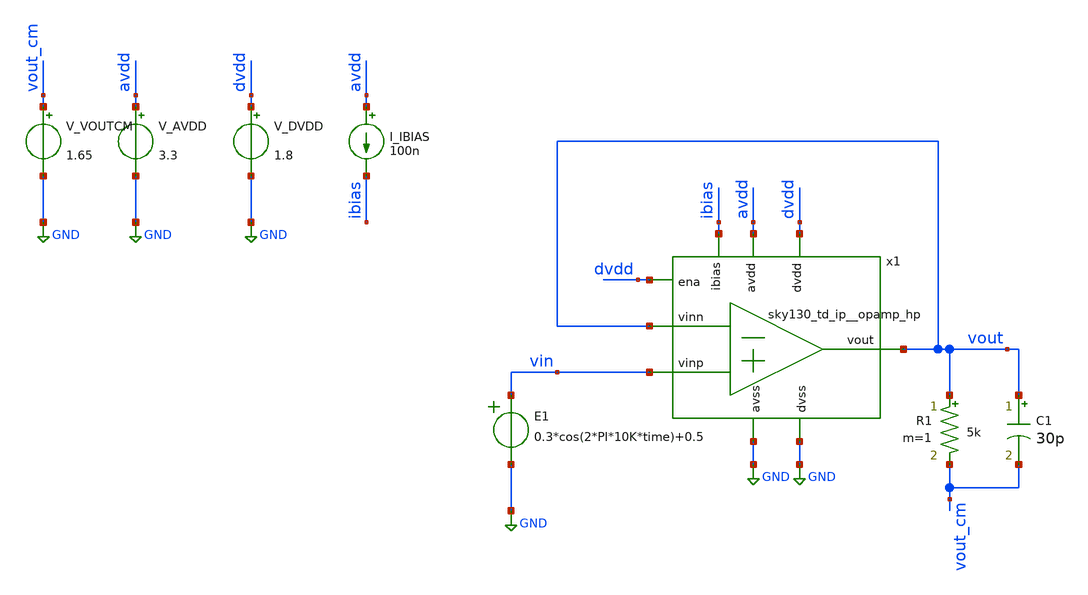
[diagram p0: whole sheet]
** sch_path: cace/output_swing.sch
**.subckt output_swing
x1 avdd vout ibias vout vin GND dvdd GND dvdd sky130_td_ip__opamp_hp
V_AVDD avdd GND 3.3
.save i(v_avdd)
V_DVDD dvdd GND 1.8
.save i(v_dvdd)
I_IBIAS avdd ibias 100n
R1 vout vout_cm 5k m=1
C1 vout vout_cm 30p m=1
V_VOUTCM vout_cm GND 1.65
.save i(v_voutcm)
E1 vin GND VOL=' 0.3*cos(2*PI*10K*time)+0.5 '
**** begin user architecture code


.save all

.control
save all

tran 100n 1m
run

fourier 10e3 vout

.endc




.lib /usr/local/share/pdk/sky130A/libs.tech/combined/sky130.lib.spice tt


**** end user architecture code
**.ends
.GLOBAL GND
.end
